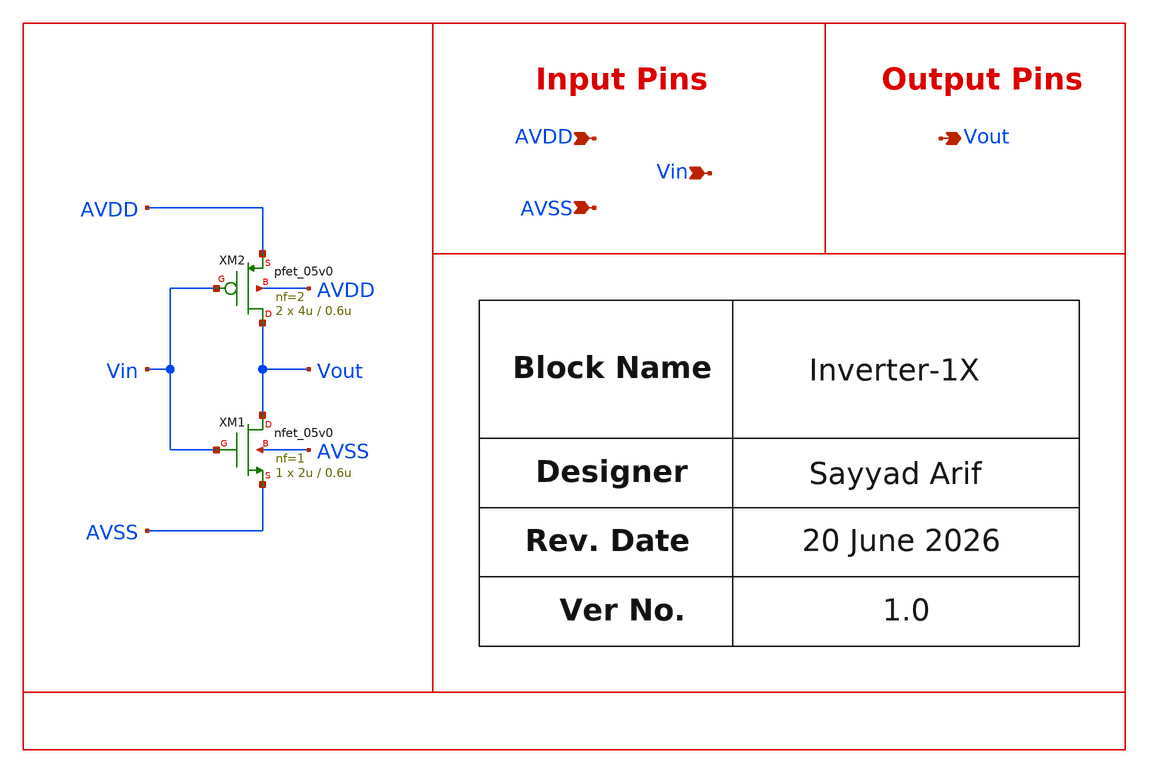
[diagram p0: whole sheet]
** sch_path: design/schematics/ADC_Buffer/sa_cic_bms_afe_iadc_quantizer_inv1x.sch
**.subckt sa_cic_bms_afe_iadc_quantizer_inv1x Vin AVDD AVSS Vout
*.ipin Vin
*.ipin AVDD
*.ipin AVSS
*.opin Vout
XM1 Vout Vin AVSS AVSS nfet_05v0 L=0.6u W=2u nf=1 ad='int((nf+1)/2) * W/nf * 0.18u' as='int((nf+2)/2) * W/nf * 0.18u'
+ pd='2*int((nf+1)/2) * (W/nf + 0.18u)' ps='2*int((nf+2)/2) * (W/nf + 0.18u)' nrd='0.18u / W' nrs='0.18u / W'
+ sa=0 sb=0 sd=0 m=1
XM2 Vout Vin AVDD AVDD pfet_05v0 L=0.6u W=4u nf=2 ad='int((nf+1)/2) * W/nf * 0.18u' as='int((nf+2)/2) * W/nf * 0.18u'
+ pd='2*int((nf+1)/2) * (W/nf + 0.18u)' ps='2*int((nf+2)/2) * (W/nf + 0.18u)' nrd='0.18u / W' nrs='0.18u / W'
+ sa=0 sb=0 sd=0 m=2
**.ends
.end
